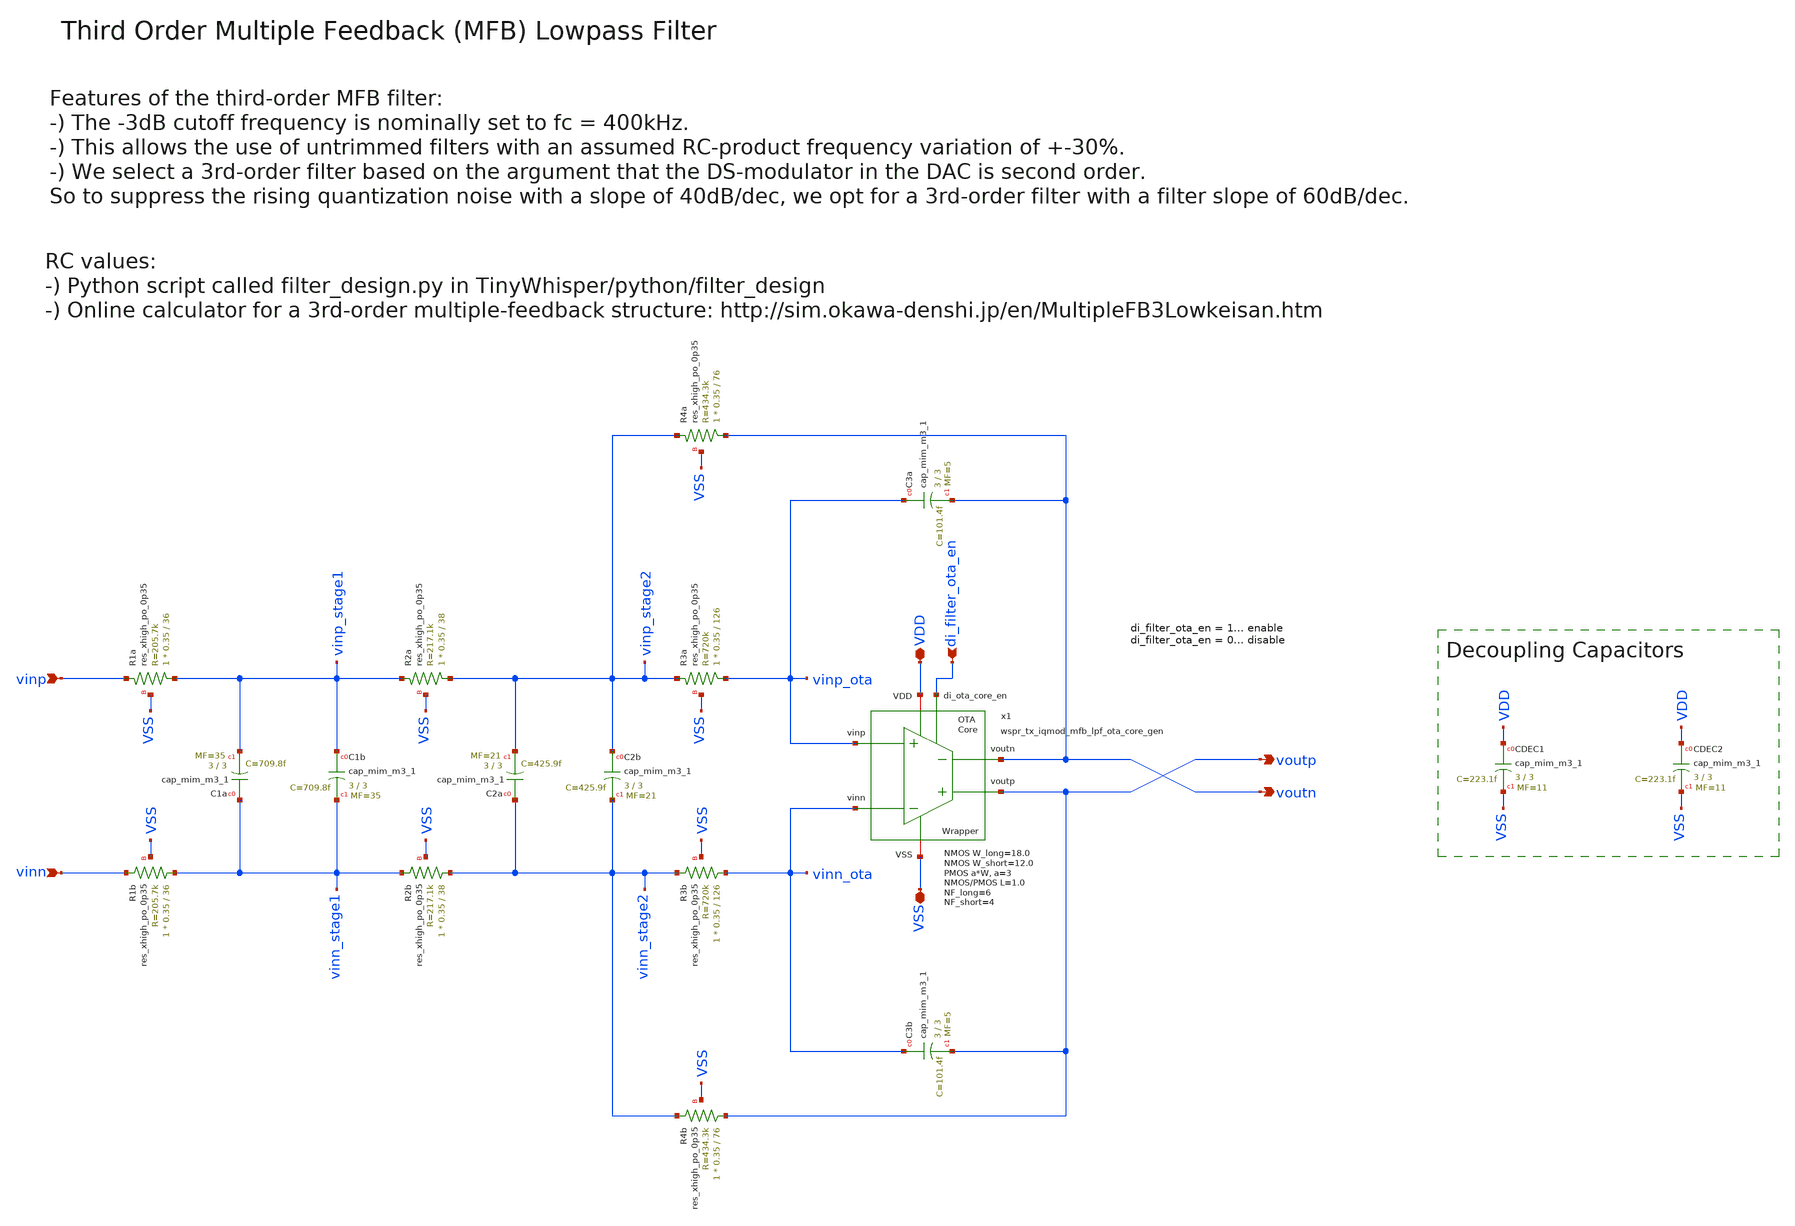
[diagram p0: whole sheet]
** sch_path: sky130/xschem/generic/wspr_tx_iqmod_mfb_lpf_gen.sch
**.subckt wspr_tx_iqmod_mfb_lpf_gen VDD VSS di_filter_ota_en vinp vinn voutp voutn
*.iopin VDD
*.iopin VSS
*.ipin di_filter_ota_en
*.ipin vinp
*.ipin vinn
*.opin voutp
*.opin voutn
XC3a vinp_ota voutn sky130_fd_pr__cap_mim_m3_1 W=3 L=3 MF=5 m=5
XC3b vinn_ota voutp sky130_fd_pr__cap_mim_m3_1 W=3 L=3 MF=5 m=5
XC1b vinp_stage1 vinn_stage1 sky130_fd_pr__cap_mim_m3_1 W=3 L=3 MF=35 m=35
XC2b vinp_stage2 vinn_stage2 sky130_fd_pr__cap_mim_m3_1 W=3 L=3 MF=21 m=21
XR1a vinp_stage1 vinp VSS sky130_fd_pr__res_xhigh_po_0p35 L=36 mult=1 m=1
XR2a vinp_stage2 vinp_stage1 VSS sky130_fd_pr__res_xhigh_po_0p35 L=38 mult=1 m=1
XR3a vinp_ota vinp_stage2 VSS sky130_fd_pr__res_xhigh_po_0p35 L=126 mult=1 m=1
XR4a voutn vinp_stage2 VSS sky130_fd_pr__res_xhigh_po_0p35 L=76 mult=1 m=1
XR1b vinn_stage1 vinn VSS sky130_fd_pr__res_xhigh_po_0p35 L=36 mult=1 m=1
XR2b vinn_stage2 vinn_stage1 VSS sky130_fd_pr__res_xhigh_po_0p35 L=38 mult=1 m=1
XR3b vinn_ota vinn_stage2 VSS sky130_fd_pr__res_xhigh_po_0p35 L=126 mult=1 m=1
XR4b voutp vinn_stage2 VSS sky130_fd_pr__res_xhigh_po_0p35 L=76 mult=1 m=1
XCDEC2 VDD VSS sky130_fd_pr__cap_mim_m3_1 W=3 L=3 MF=11 m=11
XCDEC1 VDD VSS sky130_fd_pr__cap_mim_m3_1 W=3 L=3 MF=11 m=11
XC1a vinn_stage1 vinp_stage1 sky130_fd_pr__cap_mim_m3_1 W=3 L=3 MF=35 m=35
XC2a vinn_stage2 vinp_stage2 sky130_fd_pr__cap_mim_m3_1 W=3 L=3 MF=21 m=21
x1 di_filter_ota_en voutp voutn vinn_ota vinp_ota VDD VSS wspr_tx_iqmod_mfb_lpf_ota_core_gen
+ W_long=18.0 W_short=12.0 a=3 L=1.0 NF_long=6 NF_short=4
**.ends
.end
